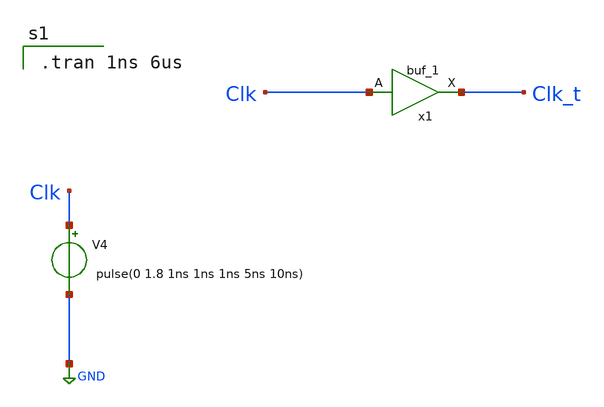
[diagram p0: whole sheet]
** sch_path: adc_comp/untitled.sch
**.subckt untitled
x1 Clk VSS VNB VPB VDD Clk_t sky130_fd_sc_hd__buf_1
V4 Clk GND pulse(0 1.8 1ns 1ns 1ns 5ns 10ns)
**** begin user architecture code

** opencircuitdesign pdks install
.lib $::SKYWATER_MODELS/sky130.lib.spice tt
.include $::SKYWATER_STDCELLS/sky130_fd_sc_hd.spice


.tran 1ns 6us

**** end user architecture code
**.ends
.GLOBAL GND
.end
